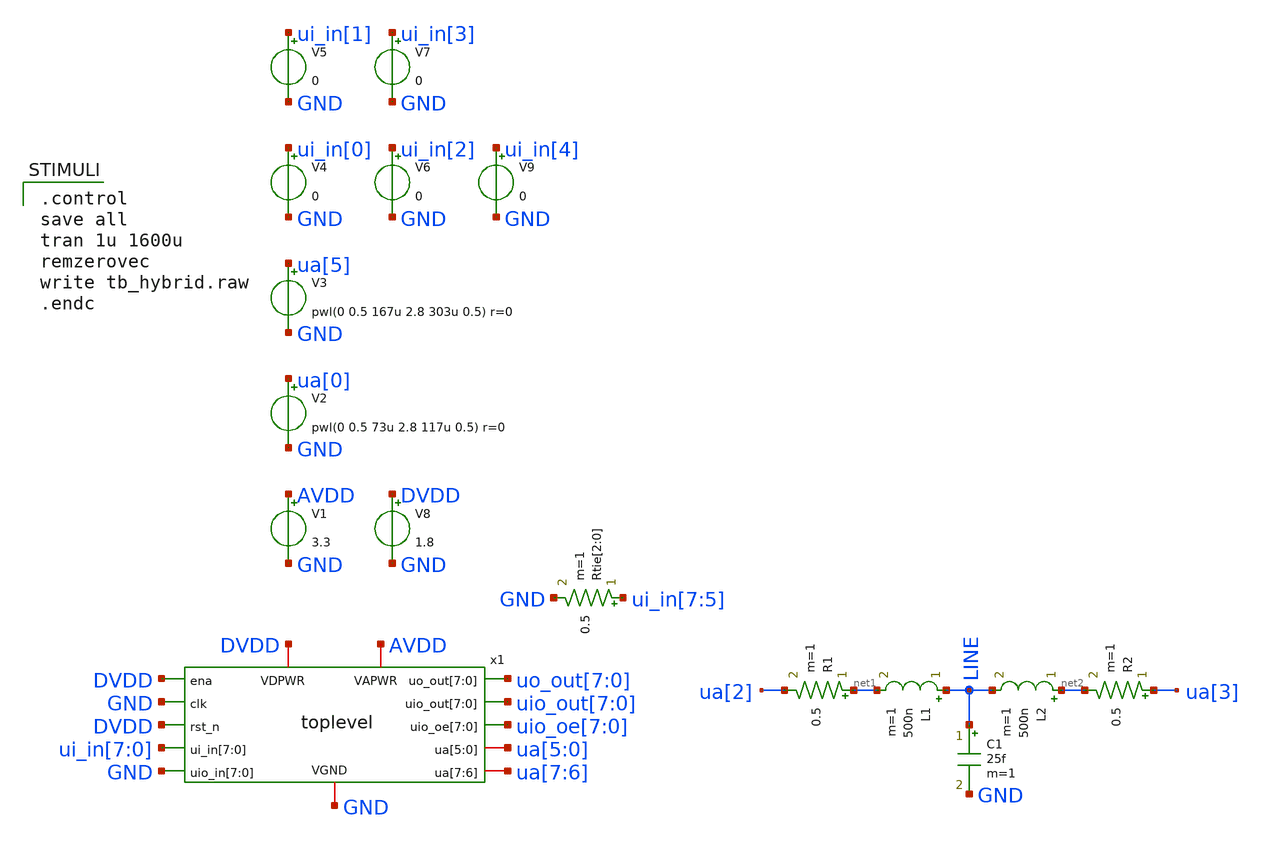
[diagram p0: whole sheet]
** sch_path: xschem/tb_toplevel.sch
**.subckt tb_toplevel
V1 AVDD GND 3.3
V2 ua[0] GND pwl(0 0.5 73u 2.8 117u 0.5) r=0
V3 ua[5] GND pwl(0 0.5 167u 2.8 303u 0.5) r=0
V4 ui_in[0] GND 0
V5 ui_in[1] GND 0
V6 ui_in[2] GND 0
V7 ui_in[3] GND 0
L1 LINE net1 500n m=1
R1 net1 ua[2] 0.5 m=1
R2 ua[3] net2 0.5 m=1
L2 net2 LINE 500n m=1
C1 LINE GND 25f m=1
V8 DVDD GND 1.8
x1 uo_out[7] uo_out[6] uo_out[5] uo_out[4] uo_out[3] uo_out[2] uo_out[1] uo_out[0] DVDD GND
+ uio_out[7] uio_out[6] uio_out[5] uio_out[4] uio_out[3] uio_out[2] uio_out[1] uio_out[0] DVDD uio_oe[7]
+ uio_oe[6] uio_oe[5] uio_oe[4] uio_oe[3] uio_oe[2] uio_oe[1] uio_oe[0] ui_in[7] ui_in[6] ui_in[5] ui_in[4]
+ ui_in[3] ui_in[2] ui_in[1] ui_in[0] GND GND GND GND GND GND GND GND ua[5] ua[4] ua[3] ua[2] ua[1] ua[0]
+ ua[7] ua[6] AVDD DVDD GND toplevel
Rtie[2] ui_in[7] GND 0.5 m=1
Rtie[1] ui_in[6] GND 0.5 m=1
Rtie[0] ui_in[5] GND 0.5 m=1
V9 ui_in[4] GND 0
**** begin user architecture code

.control
save all
tran 1u 1600u
remzerovec
write tb_hybrid.raw
.endc


 .lib $::SKYWATER_MODELS/sky130.lib.spice tt
.include $::SKYWATER_STDCELLS/sky130_fd_sc_hd.spice

**** end user architecture code
**.ends

* expanding   symbol:  toplevel.sym # of pins=13
** sym_path: xschem/toplevel.sym
** sch_path: xschem/toplevel.sch
.subckt toplevel uo_out[7] uo_out[6] uo_out[5] uo_out[4] uo_out[3] uo_out[2] uo_out[1] uo_out[0] ena
+ clk uio_out[7] uio_out[6] uio_out[5] uio_out[4] uio_out[3] uio_out[2] uio_out[1] uio_out[0] rst_n
+ uio_oe[7] uio_oe[6] uio_oe[5] uio_oe[4] uio_oe[3] uio_oe[2] uio_oe[1] uio_oe[0] ui_in[7] ui_in[6] ui_in[5]
+ ui_in[4] ui_in[3] ui_in[2] ui_in[1] ui_in[0] uio_in[7] uio_in[6] uio_in[5] uio_in[4] uio_in[3] uio_in[2]
+ uio_in[1] uio_in[0] ua[5] ua[4] ua[3] ua[2] ua[1] ua[0] ua[7] ua[6] VAPWR VDPWR VGND
*.ipin ena
*.ipin clk
*.ipin rst_n
*.ipin ui_in[7],ui_in[6],ui_in[5],ui_in[4],ui_in[3],ui_in[2],ui_in[1],ui_in[0]
*.ipin uio_in[7],uio_in[6],uio_in[5],uio_in[4],uio_in[3],uio_in[2],uio_in[1],uio_in[0]
*.opin uo_out[7],uo_out[6],uo_out[5],uo_out[4],uo_out[3],uo_out[2],uo_out[1],uo_out[0]
*.opin uio_out[7],uio_out[6],uio_out[5],uio_out[4],uio_out[3],uio_out[2],uio_out[1],uio_out[0]
*.opin uio_oe[7],uio_oe[6],uio_oe[5],uio_oe[4],uio_oe[3],uio_oe[2],uio_oe[1],uio_oe[0]
*.iopin VAPWR
*.iopin VDPWR
*.iopin VGND
*.iopin ua[5],ua[4],ua[3],ua[2],ua[1],ua[0]
*.iopin ua[7],ua[6]
x1 VAPWR ua[0] ua[2] ua[1] VGND hybrid
x2 VAPWR ua[5] ua[3] ui_in_3v3[3] ui_in_3v3[2] ui_in_3v3[1] ui_in_3v3[0] ua[4] VGND hybrid_ctrl
x3 VAPWR ua[2] ua[3] ui_in_3v3[4] VGND passgate
xsi[7] VAPWR VDPWR ui_in_3v3[7] ui_in[7] VGND level_shifter
xsi[6] VAPWR VDPWR ui_in_3v3[6] ui_in[6] VGND level_shifter
xsi[5] VAPWR VDPWR ui_in_3v3[5] ui_in[5] VGND level_shifter
xsi[4] VAPWR VDPWR ui_in_3v3[4] ui_in[4] VGND level_shifter
xsi[3] VAPWR VDPWR ui_in_3v3[3] ui_in[3] VGND level_shifter
xsi[2] VAPWR VDPWR ui_in_3v3[2] ui_in[2] VGND level_shifter
xsi[1] VAPWR VDPWR ui_in_3v3[1] ui_in[1] VGND level_shifter
xsi[0] VAPWR VDPWR ui_in_3v3[0] ui_in[0] VGND level_shifter
* noconn ena
* noconn clk
* noconn rst_n
* noconn uio_in[7:0]
* noconn ua[7:6]
xso[7] VDPWR VAPWR uo_out[7] decoder_out[7] VGND level_shifter
xso[6] VDPWR VAPWR uo_out[6] decoder_out[6] VGND level_shifter
xso[5] VDPWR VAPWR uo_out[5] decoder_out[5] VGND level_shifter
xso[4] VDPWR VAPWR uo_out[4] decoder_out[4] VGND level_shifter
xso[3] VDPWR VAPWR uo_out[3] decoder_out[3] VGND level_shifter
xso[2] VDPWR VAPWR uo_out[2] decoder_out[2] VGND level_shifter
xso[1] VDPWR VAPWR uo_out[1] decoder_out[1] VGND level_shifter
xso[0] VDPWR VAPWR uo_out[0] decoder_out[0] VGND level_shifter
xsio[7] VDPWR VAPWR uio_out[7] decoder_out[15] VGND level_shifter
xsio[6] VDPWR VAPWR uio_out[6] decoder_out[14] VGND level_shifter
xsio[5] VDPWR VAPWR uio_out[5] decoder_out[13] VGND level_shifter
xsio[4] VDPWR VAPWR uio_out[4] decoder_out[12] VGND level_shifter
xsio[3] VDPWR VAPWR uio_out[3] decoder_out[11] VGND level_shifter
xsio[2] VDPWR VAPWR uio_out[2] decoder_out[10] VGND level_shifter
xsio[1] VDPWR VAPWR uio_out[1] decoder_out[9] VGND level_shifter
xsio[0] VDPWR VAPWR uio_out[0] decoder_out[8] VGND level_shifter
x4 VAPWR ui_in_3v3[7] ui_in_3v3[6] ui_in_3v3[5] ui_in_3v3[4] decoder_out[15] decoder_out[14]
+ decoder_out[13] decoder_out[12] decoder_out[11] decoder_out[10] decoder_out[9] decoder_out[8] decoder_out[7]
+ decoder_out[6] decoder_out[5] decoder_out[4] decoder_out[3] decoder_out[2] decoder_out[1] decoder_out[0] VGND
+ decoder4_signed
xtie[7] VDPWR uio_oe[7] VGND tie_high
xtie[6] VDPWR uio_oe[6] VGND tie_high
xtie[5] VDPWR uio_oe[5] VGND tie_high
xtie[4] VDPWR uio_oe[4] VGND tie_high
xtie[3] VDPWR uio_oe[3] VGND tie_high
xtie[2] VDPWR uio_oe[2] VGND tie_high
xtie[1] VDPWR uio_oe[1] VGND tie_high
xtie[0] VDPWR uio_oe[0] VGND tie_high
.ends


* expanding   symbol:  hybrid.sym # of pins=5
** sym_path: xschem/hybrid.sym
** sch_path: xschem/hybrid.sch
.subckt hybrid VDD IN LINE OUT VSS
*.iopin VDD
*.iopin VSS
*.ipin IN
*.opin OUT
*.iopin LINE
x1 VDD OUT LINE net1 VSS opamp
XR1 IN LINE VSS sky130_fd_pr__res_xhigh_po_0p35 L=256 mult=1 m=1
XR2 IN net1 VSS sky130_fd_pr__res_xhigh_po_0p35 L=256 mult=1 m=1
XR3 net1 OUT VSS sky130_fd_pr__res_xhigh_po_0p35 L=256 mult=1 m=1
.ends


* expanding   symbol:  hybrid_ctrl.sym # of pins=6
** sym_path: xschem/hybrid_ctrl.sym
** sch_path: xschem/hybrid_ctrl.sch
.subckt hybrid_ctrl VDD IN LINE D3 D2 D1 D0 OUT VSS
*.iopin VDD
*.iopin VSS
*.ipin IN
*.opin OUT
*.iopin LINE
*.ipin D3,D2,D1,D0
x1 VDD OUT LINE net1 VSS opamp
XR1 IN LINE VSS sky130_fd_pr__res_xhigh_po_0p35 L=256 mult=1 m=1
x2 VDD D3 D2 D1 D0 IN net1 OUT VSS digipot
.ends


* expanding   symbol:  passgate.sym # of pins=5
** sym_path: xschem/passgate.sym
** sch_path: xschem/passgate.sch
.subckt passgate VDD UA UB EN VSS
*.iopin VSS
*.iopin VDD
*.iopin UA
*.iopin UB
*.ipin EN
XM1 UA EN UB VSS sky130_fd_pr__nfet_g5v0d10v5 L=0.5 W=0.65 nf=1 ad='int((1 + 1)/2) * 0.65 / 1 * 0.29'
+ as='int((1 + 2)/2) * 0.65 / 1 * 0.29' pd='2*int((1 + 1)/2) * (0.65 / 1 + 0.29)' ps='2*int((1 + 2)/2) * (0.65 / 1 + 0.29)'
+ nrd='0.29 / 0.65 ' nrs='0.29 / 0.65 ' sa=0 sb=0 sd=0 mult=1 m=1
XM2 UA net1 UB VDD sky130_fd_pr__pfet_g5v0d10v5 L=0.5 W=1 nf=1 ad='int((1 + 1)/2) * 1 / 1 * 0.29' as='int((1 + 2)/2) * 1 / 1 * 0.29'
+ pd='2*int((1 + 1)/2) * (1 / 1 + 0.29)' ps='2*int((1 + 2)/2) * (1 / 1 + 0.29)' nrd='0.29 / 1 ' nrs='0.29 / 1 '
+ sa=0 sb=0 sd=0 mult=1 m=1
x1 VDD EN net1 VSS inverter
.ends


* expanding   symbol:  level_shifter.sym # of pins=5
** sym_path: xschem/level_shifter.sym
** sch_path: xschem/level_shifter.sch
.subckt level_shifter OVDD IVDD OUT IN VSS
*.iopin OVDD
*.iopin VSS
*.ipin IN
*.opin OUT
*.iopin IVDD
XM21 net1 IN VSS VSS sky130_fd_pr__nfet_g5v0d10v5 L=0.5 W=0.65 nf=1 ad='int((1 + 1)/2) * 0.65 / 1 * 0.29'
+ as='int((1 + 2)/2) * 0.65 / 1 * 0.29' pd='2*int((1 + 1)/2) * (0.65 / 1 + 0.29)' ps='2*int((1 + 2)/2) * (0.65 / 1 + 0.29)'
+ nrd='0.29 / 0.65 ' nrs='0.29 / 0.65 ' sa=0 sb=0 sd=0 mult=1 m=1
XM25 net1 OUT OVDD OVDD sky130_fd_pr__pfet_g5v0d10v5 L=0.5 W=1 nf=1 ad='int((1 + 1)/2) * 1 / 1 * 0.29'
+ as='int((1 + 2)/2) * 1 / 1 * 0.29' pd='2*int((1 + 1)/2) * (1 / 1 + 0.29)' ps='2*int((1 + 2)/2) * (1 / 1 + 0.29)'
+ nrd='0.29 / 1 ' nrs='0.29 / 1 ' sa=0 sb=0 sd=0 mult=1 m=1
XM1 OUT net1 OVDD OVDD sky130_fd_pr__pfet_g5v0d10v5 L=0.5 W=1 nf=1 ad='int((1 + 1)/2) * 1 / 1 * 0.29'
+ as='int((1 + 2)/2) * 1 / 1 * 0.29' pd='2*int((1 + 1)/2) * (1 / 1 + 0.29)' ps='2*int((1 + 2)/2) * (1 / 1 + 0.29)'
+ nrd='0.29 / 1 ' nrs='0.29 / 1 ' sa=0 sb=0 sd=0 mult=1 m=1
XM2 OUT IN_B VSS VSS sky130_fd_pr__nfet_g5v0d10v5 L=0.5 W=0.65 nf=1 ad='int((1 + 1)/2) * 0.65 / 1 * 0.29'
+ as='int((1 + 2)/2) * 0.65 / 1 * 0.29' pd='2*int((1 + 1)/2) * (0.65 / 1 + 0.29)' ps='2*int((1 + 2)/2) * (0.65 / 1 + 0.29)'
+ nrd='0.29 / 0.65 ' nrs='0.29 / 0.65 ' sa=0 sb=0 sd=0 mult=1 m=1
x1 IVDD IN IN_B VSS inverter
.ends


* expanding   symbol:  decoder4_signed.sym # of pins=4
** sym_path: xschem/decoder4_signed.sym
** sch_path: xschem/decoder4_signed.sch
.subckt decoder4_signed VDD D3 D2 D1 D0 U15 U14 U13 U12 U11 U10 U9 U8 U7 U6 U5 U4 U3 U2 U1 U0 VSS
*.iopin VDD
*.iopin VSS
*.opin U15,U14,U13,U12,U11,U10,U9,U8,U7,U6,U5,U4,U3,U2,U1,U0
*.ipin D3,D2,D1,D0
x1 VDD D0 D3 net4 net3 net1 net2 VSS VDD decoder2
x2 VDD D2 D1 U14 U12 U10 U8 VSS net2 decoder2
x3 VDD D2 D1 U6 U4 U2 U0 VSS net1 decoder2
x4 VDD D2 D1 U15 U13 U11 U9 VSS net3 decoder2
x5 VDD D2 D1 U7 U5 U3 U1 VSS net4 decoder2
.ends


* expanding   symbol:  tie_high.sym # of pins=3
** sym_path: xschem/tie_high.sym
** sch_path: xschem/tie_high.sch
.subckt tie_high VDD HI VSS
*.iopin VSS
*.iopin VDD
*.opin HI
XM1 net1 net1 VSS VSS sky130_fd_pr__nfet_g5v0d10v5 L=0.5 W=0.65 nf=1 ad='int((1 + 1)/2) * 0.65 / 1 * 0.29'
+ as='int((1 + 2)/2) * 0.65 / 1 * 0.29' pd='2*int((1 + 1)/2) * (0.65 / 1 + 0.29)' ps='2*int((1 + 2)/2) * (0.65 / 1 + 0.29)'
+ nrd='0.29 / 0.65 ' nrs='0.29 / 0.65 ' sa=0 sb=0 sd=0 mult=1 m=1
XM2 HI net1 VDD VDD sky130_fd_pr__pfet_g5v0d10v5 L=0.5 W=1 nf=1 ad='int((1 + 1)/2) * 1 / 1 * 0.29' as='int((1 + 2)/2) * 1 / 1 * 0.29'
+ pd='2*int((1 + 1)/2) * (1 / 1 + 0.29)' ps='2*int((1 + 2)/2) * (1 / 1 + 0.29)' nrd='0.29 / 1 ' nrs='0.29 / 1 '
+ sa=0 sb=0 sd=0 mult=1 m=1
.ends


* expanding   symbol:  opamp.sym # of pins=5
** sym_path: xschem/opamp.sym
** sch_path: xschem/opamp.sch
.subckt opamp VDD OUT P N VSS
*.iopin VDD
*.iopin VSS
*.ipin P
*.ipin N
*.opin OUT
XR1 net2 VDD VSS sky130_fd_pr__res_xhigh_po_0p35 L=25 mult=1 m=1
XM1 net2 net2 VSS VSS sky130_fd_pr__nfet_g5v0d10v5 L=1 W=2 nf=1 ad='int((1 + 1)/2) * 2 / 1 * 0.29' as='int((1 + 2)/2) * 2 / 1 * 0.29'
+ pd='2*int((1 + 1)/2) * (2 / 1 + 0.29)' ps='2*int((1 + 2)/2) * (2 / 1 + 0.29)' nrd='0.29 / 2 ' nrs='0.29 / 2 '
+ sa=0 sb=0 sd=0 mult=2 m=2
XM7 net1 net1 VDD VDD sky130_fd_pr__pfet_g5v0d10v5 L=1 W=4 nf=1 ad='int((1 + 1)/2) * 4 / 1 * 0.29' as='int((1 + 2)/2) * 4 / 1 * 0.29'
+ pd='2*int((1 + 1)/2) * (4 / 1 + 0.29)' ps='2*int((1 + 2)/2) * (4 / 1 + 0.29)' nrd='0.29 / 4 ' nrs='0.29 / 4 '
+ sa=0 sb=0 sd=0 mult=2 m=2
XM8 OUT net1 VDD VDD sky130_fd_pr__pfet_g5v0d10v5 L=1 W=4 nf=1 ad='int((1 + 1)/2) * 4 / 1 * 0.29' as='int((1 + 2)/2) * 4 / 1 * 0.29'
+ pd='2*int((1 + 1)/2) * (4 / 1 + 0.29)' ps='2*int((1 + 2)/2) * (4 / 1 + 0.29)' nrd='0.29 / 4 ' nrs='0.29 / 4 '
+ sa=0 sb=0 sd=0 mult=2 m=2
XM4 net6 net2 VSS VSS sky130_fd_pr__nfet_g5v0d10v5 L=1 W=2 nf=1 ad='int((1 + 1)/2) * 2 / 1 * 0.29' as='int((1 + 2)/2) * 2 / 1 * 0.29'
+ pd='2*int((1 + 1)/2) * (2 / 1 + 0.29)' ps='2*int((1 + 2)/2) * (2 / 1 + 0.29)' nrd='0.29 / 2 ' nrs='0.29 / 2 '
+ sa=0 sb=0 sd=0 mult=2 m=2
XM5 net1 P net6 VSS sky130_fd_pr__nfet_g5v0d10v5 L=1 W=2 nf=1 ad='int((1 + 1)/2) * 2 / 1 * 0.29' as='int((1 + 2)/2) * 2 / 1 * 0.29'
+ pd='2*int((1 + 1)/2) * (2 / 1 + 0.29)' ps='2*int((1 + 2)/2) * (2 / 1 + 0.29)' nrd='0.29 / 2 ' nrs='0.29 / 2 '
+ sa=0 sb=0 sd=0 mult=2 m=2
XM6 OUT N net6 VSS sky130_fd_pr__nfet_g5v0d10v5 L=1 W=2 nf=1 ad='int((1 + 1)/2) * 2 / 1 * 0.29' as='int((1 + 2)/2) * 2 / 1 * 0.29'
+ pd='2*int((1 + 1)/2) * (2 / 1 + 0.29)' ps='2*int((1 + 2)/2) * (2 / 1 + 0.29)' nrd='0.29 / 2 ' nrs='0.29 / 2 '
+ sa=0 sb=0 sd=0 mult=2 m=2
XM2 net5 net2 VSS VSS sky130_fd_pr__nfet_g5v0d10v5 L=1 W=2 nf=1 ad='int((1 + 1)/2) * 2 / 1 * 0.29' as='int((1 + 2)/2) * 2 / 1 * 0.29'
+ pd='2*int((1 + 1)/2) * (2 / 1 + 0.29)' ps='2*int((1 + 2)/2) * (2 / 1 + 0.29)' nrd='0.29 / 2 ' nrs='0.29 / 2 '
+ sa=0 sb=0 sd=0 mult=2 m=2
XM9 net4 net5 VDD VDD sky130_fd_pr__pfet_g5v0d10v5 L=1 W=4 nf=1 ad='int((1 + 1)/2) * 4 / 1 * 0.29' as='int((1 + 2)/2) * 4 / 1 * 0.29'
+ pd='2*int((1 + 1)/2) * (4 / 1 + 0.29)' ps='2*int((1 + 2)/2) * (4 / 1 + 0.29)' nrd='0.29 / 4 ' nrs='0.29 / 4 '
+ sa=0 sb=0 sd=0 mult=2 m=2
XM3 VDD net5 net5 VDD sky130_fd_pr__pfet_g5v0d10v5 L=1 W=4 nf=1 ad='int((1 + 1)/2) * 4 / 1 * 0.29' as='int((1 + 2)/2) * 4 / 1 * 0.29'
+ pd='2*int((1 + 1)/2) * (4 / 1 + 0.29)' ps='2*int((1 + 2)/2) * (4 / 1 + 0.29)' nrd='0.29 / 4 ' nrs='0.29 / 4 '
+ sa=0 sb=0 sd=0 mult=2 m=2
XM10 net3 P net4 VDD sky130_fd_pr__pfet_g5v0d10v5 L=1 W=4 nf=1 ad='int((1 + 1)/2) * 4 / 1 * 0.29' as='int((1 + 2)/2) * 4 / 1 * 0.29'
+ pd='2*int((1 + 1)/2) * (4 / 1 + 0.29)' ps='2*int((1 + 2)/2) * (4 / 1 + 0.29)' nrd='0.29 / 4 ' nrs='0.29 / 4 '
+ sa=0 sb=0 sd=0 mult=2 m=2
XM11 OUT N net4 VDD sky130_fd_pr__pfet_g5v0d10v5 L=1 W=4 nf=1 ad='int((1 + 1)/2) * 4 / 1 * 0.29' as='int((1 + 2)/2) * 4 / 1 * 0.29'
+ pd='2*int((1 + 1)/2) * (4 / 1 + 0.29)' ps='2*int((1 + 2)/2) * (4 / 1 + 0.29)' nrd='0.29 / 4 ' nrs='0.29 / 4 '
+ sa=0 sb=0 sd=0 mult=2 m=2
XM12 net3 net3 VSS VSS sky130_fd_pr__nfet_g5v0d10v5 L=1 W=2 nf=1 ad='int((1 + 1)/2) * 2 / 1 * 0.29' as='int((1 + 2)/2) * 2 / 1 * 0.29'
+ pd='2*int((1 + 1)/2) * (2 / 1 + 0.29)' ps='2*int((1 + 2)/2) * (2 / 1 + 0.29)' nrd='0.29 / 2 ' nrs='0.29 / 2 '
+ sa=0 sb=0 sd=0 mult=2 m=2
XM13 OUT net3 VSS VSS sky130_fd_pr__nfet_g5v0d10v5 L=1 W=2 nf=1 ad='int((1 + 1)/2) * 2 / 1 * 0.29' as='int((1 + 2)/2) * 2 / 1 * 0.29'
+ pd='2*int((1 + 1)/2) * (2 / 1 + 0.29)' ps='2*int((1 + 2)/2) * (2 / 1 + 0.29)' nrd='0.29 / 2 ' nrs='0.29 / 2 '
+ sa=0 sb=0 sd=0 mult=2 m=2
.ends


* expanding   symbol:  digipot.sym # of pins=6
** sym_path: xschem/digipot.sym
** sch_path: xschem/digipot.sch
.subckt digipot VDD D3 D2 D1 D0 A W B VSS
*.iopin VDD
*.iopin VSS
*.iopin A
*.iopin B
*.iopin W
*.ipin D3,D2,D1,D0
x1 VDD D3 D2 D1 D0 net1[15] net1[14] net1[13] net1[12] net1[11] net1[10] net1[9] net1[8] net1[7]
+ net1[6] net1[5] net1[4] net1[3] net1[2] net1[1] net1[0] VSS decoder4_signed
x2 VDD net1[15] net1[14] net1[13] net1[12] net1[11] net1[10] net1[9] net1[8] net1[7] net1[6] net1[5]
+ net1[4] net1[3] net1[2] net1[1] net1[0] A W B VSS digipot_1hot
.ends


* expanding   symbol:  inverter.sym # of pins=4
** sym_path: xschem/inverter.sym
** sch_path: xschem/inverter.sch
.subckt inverter VDD IN OUT VSS
*.iopin VSS
*.iopin VDD
*.ipin IN
*.opin OUT
XM1 OUT IN VSS VSS sky130_fd_pr__nfet_g5v0d10v5 L=0.5 W=0.65 nf=1 ad='int((1 + 1)/2) * 0.65 / 1 * 0.29'
+ as='int((1 + 2)/2) * 0.65 / 1 * 0.29' pd='2*int((1 + 1)/2) * (0.65 / 1 + 0.29)' ps='2*int((1 + 2)/2) * (0.65 / 1 + 0.29)'
+ nrd='0.29 / 0.65 ' nrs='0.29 / 0.65 ' sa=0 sb=0 sd=0 mult=1 m=1
XM2 OUT IN VDD VDD sky130_fd_pr__pfet_g5v0d10v5 L=0.5 W=1 nf=1 ad='int((1 + 1)/2) * 1 / 1 * 0.29' as='int((1 + 2)/2) * 1 / 1 * 0.29'
+ pd='2*int((1 + 1)/2) * (1 / 1 + 0.29)' ps='2*int((1 + 2)/2) * (1 / 1 + 0.29)' nrd='0.29 / 1 ' nrs='0.29 / 1 '
+ sa=0 sb=0 sd=0 mult=1 m=1
.ends


* expanding   symbol:  decoder2.sym # of pins=9
** sym_path: xschem/decoder2.sym
** sch_path: xschem/decoder2.sch
.subckt decoder2 VDD D1 D0 U3 U2 U1 U0 VSS EN
*.iopin VDD
*.iopin VSS
*.ipin D0
*.ipin D1
*.opin U0
*.opin U1
*.opin U2
*.opin U3
*.ipin EN
x6 VDD net5 net4 U0 net3 VSS nor3
x7 VDD net5 net1 U1 net3 VSS nor3
x8 VDD net2 net4 U2 net3 VSS nor3
x9 VDD net2 net1 U3 net3 VSS nor3
x1 VDD EN net3 VSS inverter
x2 VDD D0 net1 VSS inverter
x3 VDD net1 net4 VSS inverter
x4 VDD D1 net2 VSS inverter
x5 VDD net2 net5 VSS inverter
.ends


* expanding   symbol:  digipot_1hot.sym # of pins=6
** sym_path: xschem/digipot_1hot.sym
** sch_path: xschem/digipot_1hot.sch
.subckt digipot_1hot VDD U15 U14 U13 U12 U11 U10 U9 U8 U7 U6 U5 U4 U3 U2 U1 U0 A W B VSS
*.iopin VDD
*.iopin VSS
*.iopin A
*.iopin B
*.iopin W
*.ipin U15,U14,U13,U12,U11,U10,U9,U8,U7,U6,U5,U4,U3,U2,U1,U0
XR1 A net1 VSS sky130_fd_pr__res_xhigh_po_0p35 L=32 mult=1 m=1
XR2 net1 net2 VSS sky130_fd_pr__res_xhigh_po_0p35 L=32 mult=1 m=1
XR3 net2 net3 VSS sky130_fd_pr__res_xhigh_po_0p35 L=32 mult=1 m=1
XR4 net3 net4 VSS sky130_fd_pr__res_xhigh_po_0p35 L=32 mult=1 m=1
XR5 net4 net5 VSS sky130_fd_pr__res_xhigh_po_0p35 L=32 mult=1 m=1
x1 VDD A W U0 VSS passgate
x2 VDD net1 W U1 VSS passgate
x3 VDD net2 W U2 VSS passgate
x4 VDD net3 W U3 VSS passgate
x5 VDD net4 W U4 VSS passgate
XR6 net5 net6 VSS sky130_fd_pr__res_xhigh_po_0p35 L=32 mult=1 m=1
x6 VDD net5 W U5 VSS passgate
XR7 net6 net7 VSS sky130_fd_pr__res_xhigh_po_0p35 L=32 mult=1 m=1
x7 VDD net6 W U6 VSS passgate
XR8 net8 net7 VSS sky130_fd_pr__res_xhigh_po_0p35 L=32 mult=1 m=1
x8 VDD net7 W U7 VSS passgate
XR9 net8 net9 VSS sky130_fd_pr__res_xhigh_po_0p35 L=32 mult=1 m=1
XR10 net9 net10 VSS sky130_fd_pr__res_xhigh_po_0p35 L=32 mult=1 m=1
XR11 net10 net11 VSS sky130_fd_pr__res_xhigh_po_0p35 L=32 mult=1 m=1
XR12 net11 net12 VSS sky130_fd_pr__res_xhigh_po_0p35 L=32 mult=1 m=1
XR13 net12 net13 VSS sky130_fd_pr__res_xhigh_po_0p35 L=32 mult=1 m=1
x9 VDD net8 W U8 VSS passgate
x10 VDD net9 W U9 VSS passgate
x11 VDD net10 W U10 VSS passgate
x12 VDD net11 W U11 VSS passgate
x13 VDD net12 W U12 VSS passgate
XR14 net13 net14 VSS sky130_fd_pr__res_xhigh_po_0p35 L=32 mult=1 m=1
x14 VDD net13 W U13 VSS passgate
XR15 net14 net15 VSS sky130_fd_pr__res_xhigh_po_0p35 L=32 mult=1 m=1
x15 VDD net14 W U14 VSS passgate
x16 VDD net15 W U15 VSS passgate
XR16 B net15 VSS sky130_fd_pr__res_xhigh_po_0p35 L=32 mult=1 m=1
.ends


* expanding   symbol:  nor3.sym # of pins=6
** sym_path: xschem/nor3.sym
** sch_path: xschem/nor3.sch
.subckt nor3 VDD A B OUT C VSS
*.iopin VSS
*.iopin VDD
*.ipin B
*.ipin A
*.ipin C
*.opin OUT
XM2 OUT B VSS VSS sky130_fd_pr__nfet_g5v0d10v5 L=0.5 W=0.65 nf=1 ad='int((1 + 1)/2) * 0.65 / 1 * 0.29'
+ as='int((1 + 2)/2) * 0.65 / 1 * 0.29' pd='2*int((1 + 1)/2) * (0.65 / 1 + 0.29)' ps='2*int((1 + 2)/2) * (0.65 / 1 + 0.29)'
+ nrd='0.29 / 0.65 ' nrs='0.29 / 0.65 ' sa=0 sb=0 sd=0 mult=1 m=1
XM1 OUT A VSS VSS sky130_fd_pr__nfet_g5v0d10v5 L=0.5 W=0.65 nf=1 ad='int((1 + 1)/2) * 0.65 / 1 * 0.29'
+ as='int((1 + 2)/2) * 0.65 / 1 * 0.29' pd='2*int((1 + 1)/2) * (0.65 / 1 + 0.29)' ps='2*int((1 + 2)/2) * (0.65 / 1 + 0.29)'
+ nrd='0.29 / 0.65 ' nrs='0.29 / 0.65 ' sa=0 sb=0 sd=0 mult=1 m=1
XM4 net1 A VDD VDD sky130_fd_pr__pfet_g5v0d10v5 L=0.5 W=1 nf=1 ad='int((1 + 1)/2) * 1 / 1 * 0.29' as='int((1 + 2)/2) * 1 / 1 * 0.29'
+ pd='2*int((1 + 1)/2) * (1 / 1 + 0.29)' ps='2*int((1 + 2)/2) * (1 / 1 + 0.29)' nrd='0.29 / 1 ' nrs='0.29 / 1 '
+ sa=0 sb=0 sd=0 mult=1 m=1
XM3 OUT C VSS VSS sky130_fd_pr__nfet_g5v0d10v5 L=0.5 W=0.65 nf=1 ad='int((1 + 1)/2) * 0.65 / 1 * 0.29'
+ as='int((1 + 2)/2) * 0.65 / 1 * 0.29' pd='2*int((1 + 1)/2) * (0.65 / 1 + 0.29)' ps='2*int((1 + 2)/2) * (0.65 / 1 + 0.29)'
+ nrd='0.29 / 0.65 ' nrs='0.29 / 0.65 ' sa=0 sb=0 sd=0 mult=1 m=1
XM5 net2 B net1 VDD sky130_fd_pr__pfet_g5v0d10v5 L=0.5 W=1 nf=1 ad='int((1 + 1)/2) * 1 / 1 * 0.29' as='int((1 + 2)/2) * 1 / 1 * 0.29'
+ pd='2*int((1 + 1)/2) * (1 / 1 + 0.29)' ps='2*int((1 + 2)/2) * (1 / 1 + 0.29)' nrd='0.29 / 1 ' nrs='0.29 / 1 '
+ sa=0 sb=0 sd=0 mult=1 m=1
XM6 OUT C net2 VDD sky130_fd_pr__pfet_g5v0d10v5 L=0.5 W=1 nf=1 ad='int((1 + 1)/2) * 1 / 1 * 0.29' as='int((1 + 2)/2) * 1 / 1 * 0.29'
+ pd='2*int((1 + 1)/2) * (1 / 1 + 0.29)' ps='2*int((1 + 2)/2) * (1 / 1 + 0.29)' nrd='0.29 / 1 ' nrs='0.29 / 1 '
+ sa=0 sb=0 sd=0 mult=1 m=1
.ends

.end
